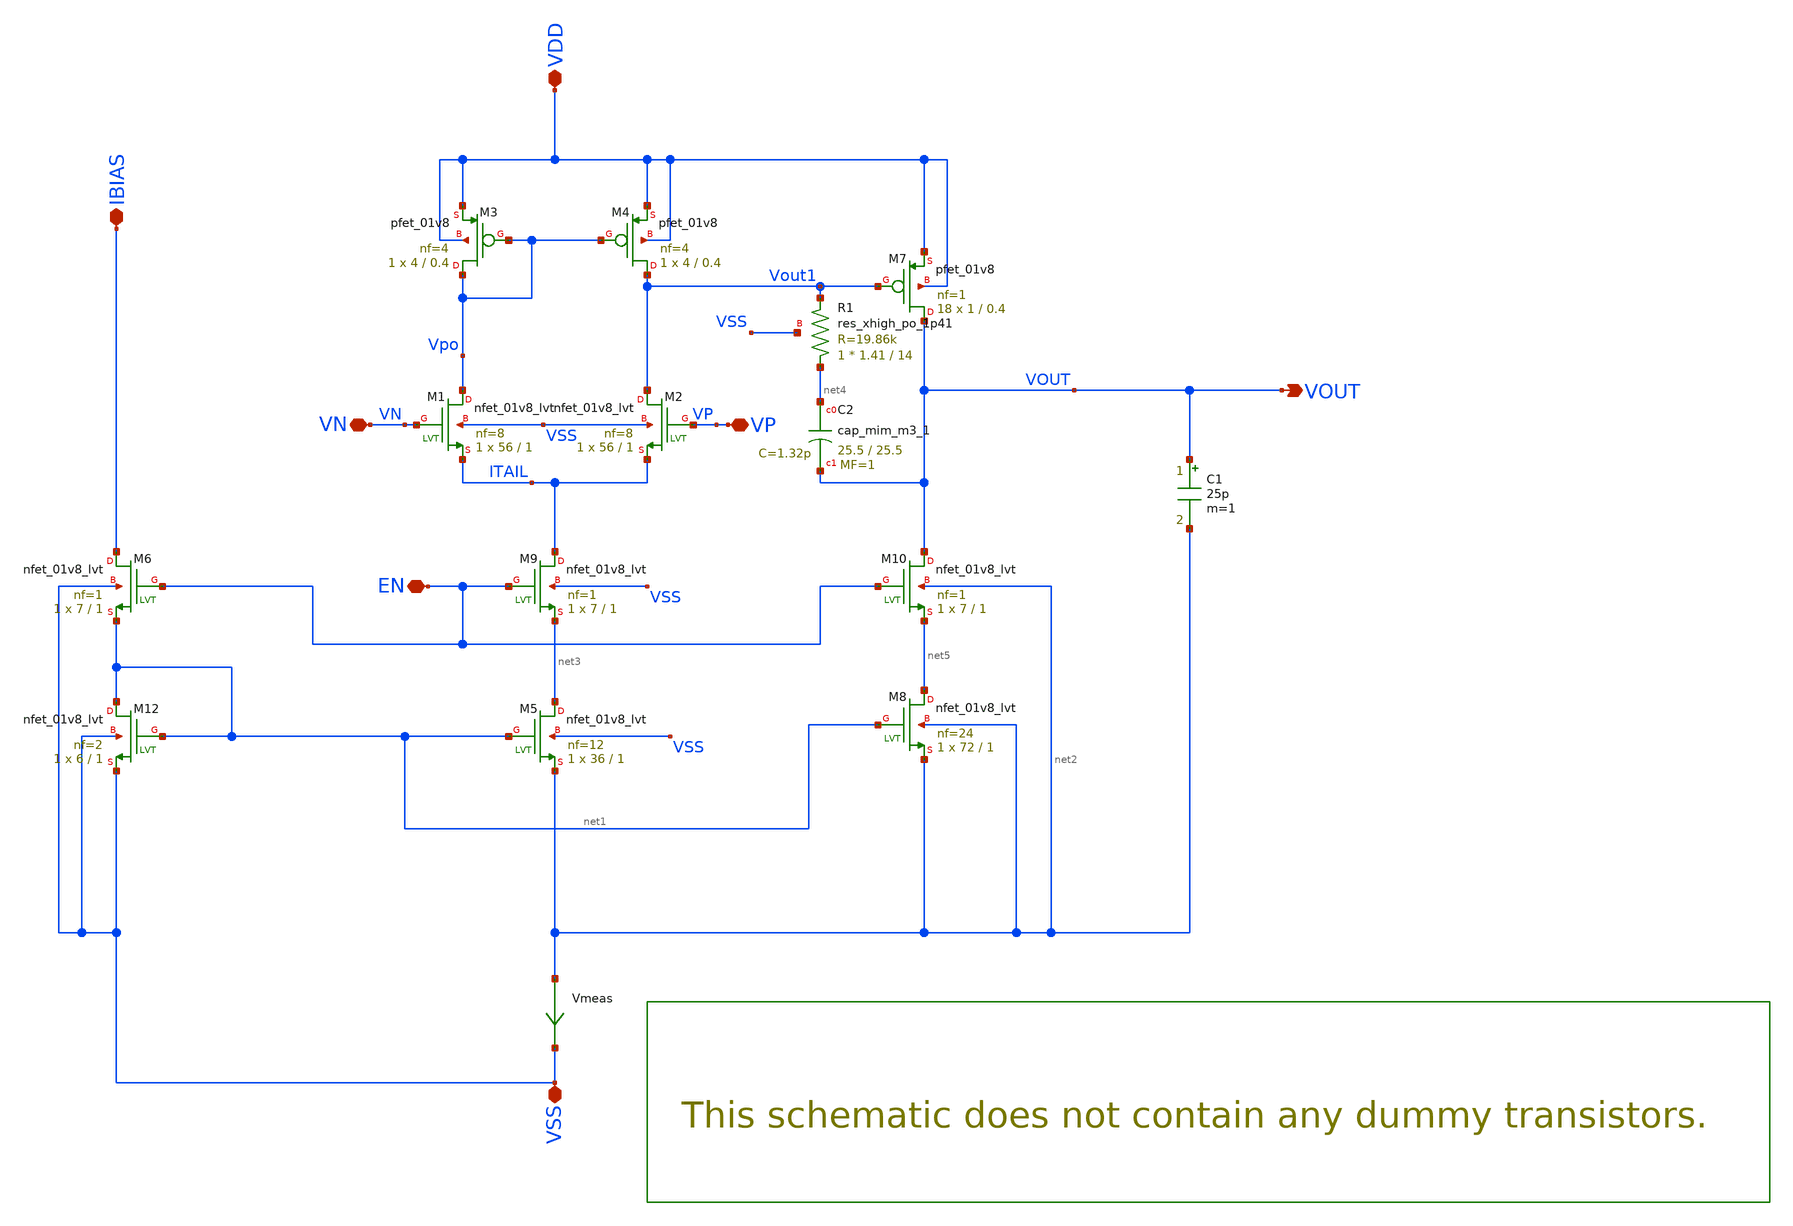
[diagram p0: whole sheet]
** sch_path: xschem/ttsky25_two_stage_opamp_tb.sch
**.subckt ttsky25_two_stage_opamp_tb VSS VDD IBIAS VOUT EN VN VP
*.iopin VSS
*.iopin VDD
*.iopin IBIAS
*.opin VOUT
*.iopin EN
*.iopin VN
*.iopin VP
C1 VOUT net2 25p m=1
XM7 VOUT Vout1 VDD VDD sky130_fd_pr__pfet_01v8 L=0.4 W=1 nf=1 ad='int((nf+1)/2) * W/nf * 0.29' as='int((nf+2)/2) * W/nf * 0.29'
+ pd='2*int((nf+1)/2) * (W/nf + 0.29)' ps='2*int((nf+2)/2) * (W/nf + 0.29)' nrd='0.29 / W' nrs='0.29 / W'
+ sa=0 sb=0 sd=0 mult=18 m=18
XM4 Vout1 Vpo VDD VDD sky130_fd_pr__pfet_01v8 L=0.4 W=4 nf=4 ad='int((nf+1)/2) * W/nf * 0.29' as='int((nf+2)/2) * W/nf * 0.29'
+ pd='2*int((nf+1)/2) * (W/nf + 0.29)' ps='2*int((nf+2)/2) * (W/nf + 0.29)' nrd='0.29 / W' nrs='0.29 / W'
+ sa=0 sb=0 sd=0 mult=1 m=1
XM3 Vpo Vpo VDD VDD sky130_fd_pr__pfet_01v8 L=0.4 W=4 nf=4 ad='int((nf+1)/2) * W/nf * 0.29' as='int((nf+2)/2) * W/nf * 0.29'
+ pd='2*int((nf+1)/2) * (W/nf + 0.29)' ps='2*int((nf+2)/2) * (W/nf + 0.29)' nrd='0.29 / W' nrs='0.29 / W'
+ sa=0 sb=0 sd=0 mult=1 m=1
Vmeas net2 VSS 0
.save i(vmeas)
XM1 Vpo VN ITAIL VSS sky130_fd_pr__nfet_01v8_lvt L=1 W=56 nf=8 ad='int((8 + 1)/2) * 56 / 8 * 0.29' as='int((8 + 2)/2) * 56 / 8 * 0.29'
+ pd='2*int((8 + 1)/2) * (56 / 8 + 0.29)' ps='2*int((8 + 2)/2) * (56 / 8 + 0.29)' nrd='0.29 / 56 ' nrs='0.29 / 56 '
+ sa=0 sb=0 sd=0 mult=1 m=1
XM2 Vout1 VP ITAIL VSS sky130_fd_pr__nfet_01v8_lvt L=1 W=56 nf=8 ad='int((8 + 1)/2) * 56 / 8 * 0.29'
+ as='int((8 + 2)/2) * 56 / 8 * 0.29' pd='2*int((8 + 1)/2) * (56 / 8 + 0.29)' ps='2*int((8 + 2)/2) * (56 / 8 + 0.29)'
+ nrd='0.29 / 56 ' nrs='0.29 / 56 ' sa=0 sb=0 sd=0 mult=1 m=1
XM12 net1 net1 VSS VSS sky130_fd_pr__nfet_01v8_lvt L=1 W=6 nf=2 ad='int((2 + 1)/2) * 6 / 2 * 0.29' as='int((2 + 2)/2) * 6 / 2 * 0.29'
+ pd='2*int((2 + 1)/2) * (6 / 2 + 0.29)' ps='2*int((2 + 2)/2) * (6 / 2 + 0.29)' nrd='0.29 / 6 ' nrs='0.29 / 6 '
+ sa=0 sb=0 sd=0 mult=1 m=1
XM5 net3 net1 net2 VSS sky130_fd_pr__nfet_01v8_lvt L=1 W=36 nf=12 ad='int((12 + 1)/2) * 36 / 12 * 0.29'
+ as='int((12 + 2)/2) * 36 / 12 * 0.29' pd='2*int((12 + 1)/2) * (36 / 12 + 0.29)' ps='2*int((12 + 2)/2) * (36 / 12 + 0.29)'
+ nrd='0.29 / 36 ' nrs='0.29 / 36 ' sa=0 sb=0 sd=0 mult=1 m=1
XM8 net5 net1 net2 net2 sky130_fd_pr__nfet_01v8_lvt L=1 W=72 nf=24 ad='int((24 + 1)/2) * 72 / 24 * 0.29'
+ as='int((24 + 2)/2) * 72 / 24 * 0.29' pd='2*int((24 + 1)/2) * (72 / 24 + 0.29)' ps='2*int((24 + 2)/2) * (72 / 24 + 0.29)'
+ nrd='0.29 / 72 ' nrs='0.29 / 72 ' sa=0 sb=0 sd=0 mult=1 m=1
XM6 IBIAS EN net1 VSS sky130_fd_pr__nfet_01v8_lvt L=1 W=7 nf=1 ad='int((1 + 1)/2) * 7 / 1 * 0.29' as='int((1 + 2)/2) * 7 / 1 * 0.29'
+ pd='2*int((1 + 1)/2) * (7 / 1 + 0.29)' ps='2*int((1 + 2)/2) * (7 / 1 + 0.29)' nrd='0.29 / 7 ' nrs='0.29 / 7 '
+ sa=0 sb=0 sd=0 mult=1 m=1
XM9 ITAIL EN net3 VSS sky130_fd_pr__nfet_01v8_lvt L=1 W=7 nf=1 ad='int((1 + 1)/2) * 7 / 1 * 0.29' as='int((1 + 2)/2) * 7 / 1 * 0.29'
+ pd='2*int((1 + 1)/2) * (7 / 1 + 0.29)' ps='2*int((1 + 2)/2) * (7 / 1 + 0.29)' nrd='0.29 / 7 ' nrs='0.29 / 7 '
+ sa=0 sb=0 sd=0 mult=1 m=1
XM10 VOUT EN net5 net2 sky130_fd_pr__nfet_01v8_lvt L=1 W=7 nf=1 ad='int((1 + 1)/2) * 7 / 1 * 0.29' as='int((1 + 2)/2) * 7 / 1 * 0.29'
+ pd='2*int((1 + 1)/2) * (7 / 1 + 0.29)' ps='2*int((1 + 2)/2) * (7 / 1 + 0.29)' nrd='0.29 / 7 ' nrs='0.29 / 7 '
+ sa=0 sb=0 sd=0 mult=1 m=1
XC2 net4 VOUT sky130_fd_pr__cap_mim_m3_1 W=25.5 L=25.5 MF=1 m=1
XR1 net4 Vout1 VSS sky130_fd_pr__res_xhigh_po_1p41 L=14 mult=1 m=1
**** begin user architecture code


.lib /foss/pdks/sky130A/libs.tech/ngspice/sky130.lib.spice tt
.param vcm = 0.9
**Setup
Vdd vdd 0 1.8
Ven en 0 1.8
Ibias Vdd Ibias 5u
*Vdd vdd 0 SIN(1.8 0.1 600k)
Vss vss 0 0

*Uncomment sources below depending*
*on what simulation needs to be run*
*AC simulation or (DC + Transient)*

*This line is not really needed -> Vdiff vdiff 0 0

*Transient + DC Transfer*
*Vdiff vdiff 0 SIN(0 0.001 1k)
*Bvp vp 0 V = vcm + V(vdiff)/2
*Bvn vn 0 V = vcm - V(vdiff)/2

*AC small signal*
Vp vp 0 vcm AC 0.001
Vn vn 0 vcm AC -0.001

**Simulation
.option temp=27 gmin=1e-12
.save all
.options savecurrents
.control
** Define input signal
let fsig = 1k
let tper = 1/fsig
** Define transient params
let tstop = 10*tper
let tstep = 0.001*tper

op
remzerovec
write ttsky25_two_stage_opamp_tb.raw
echo ---xm2---
let gds2 = @m.xm2.msky130_fd_pr__nfet_01v8_lvt[gds]
let ro2 = 1/gds2
echo ---xm4---
let gds4 = @m.xm4.msky130_fd_pr__pfet_01v8[gds]
let ro4 = 1/gds4
let RoD = 1/((1/ro2) + (1/ro4))
echo ---xm6---
print @m.xm6.msky130_fd_pr__nfet_01v8_lvt[vdsat]
echo -----COMMON SOURCE-----
echo ---xm7---
let gds7 = @m.xm7.msky130_fd_pr__pfet_01v8[gds]
let gm7 = @m.xm7.msky130_fd_pr__pfet_01v8[gm]
let r_zero = 1/gm7
print r_zero
let ro7 = 1/gds7
echo ---xm8---
let gds8 = @m.xm8.msky130_fd_pr__nfet_01v8_lvt[gds]
let ro8 = 1/gds8
echo ---xm10---
let gds10 = @m.xm10.msky130_fd_pr__nfet_01v8_lvt[gds]
let ro10 = 1/gds10
let Ros = 1/((1/ro7) + (1/(ro8+ro10)))


tran $&tstep $&tstop
let current = -i(vdd)
plot vp vn vout1
plot vp vn vout

dc vdiff -0.9 0.9 10m
let vin = vp -vn
plot vin vout1 vdd
meas dc vout1_at_zero find vout1 when vdiff=0

dc vdiff -0.9 0.9 10m
let vin = vp -vn
plot vin vout vdd
meas dc vout_at_zero find vout when vdiff=0

ac dec 200 10 10000Meg
let vin = vp - vn
let gain = db(vout/vin)
let phase_deg = 180*cph(vout/vin)/pi
plot gain phase_deg xlog
meas ac gain_max MAX gain
let db_3 = gain_max - 3
print db_3
meas ac f_pole WHEN gain = db_3
meas ac f_u WHEN gain = 0
meas ac gain_10k FIND gain AT=10e3
meas ac phase_at_fu FIND phase_deg AT=f_u
let phase_margin = 180 + phase_at_fu
print phase_margin
setplot op1
print @m.xm2.msky130_fd_pr__nfet_01v8_lvt[vth]
print @m.xm2.msky130_fd_pr__nfet_01v8_lvt[gm]
print @m.xm2.msky130_fd_pr__nfet_01v8_lvt[vdsat]
print @m.xm7.msky130_fd_pr__pfet_01v8[vth]
print @m.xm7.msky130_fd_pr__pfet_01v8[gm]
print @m.xm7.msky130_fd_pr__pfet_01v8[vdsat]
print @m.xm4.msky130_fd_pr__pfet_01v8[vth]
print @m.xm4.msky130_fd_pr__pfet_01v8[gm]
print @m.xm4.msky130_fd_pr__pfet_01v8[vdsat]
print ro2
print ro4
print RoD
print ro10
print ro8
print ro8+ro10
print ro7
print Ros
let ro5 = 1/@m.xm5.msky130_fd_pr__nfet_01v8_lvt[gds]
print ro5
let Av1 = @m.xm2.msky130_fd_pr__nfet_01v8_lvt[gm] * RoD
let Av2 = @m.xm7.msky130_fd_pr__pfet_01v8[gm] * Ros
print Av1
print Av2
let x7_gm_id = @m.xm7.msky130_fd_pr__pfet_01v8[gm]/@m.xm7.msky130_fd_pr__pfet_01v8[id]
print x7_gm_id
let x4_gm_id = @m.xm4.msky130_fd_pr__pfet_01v8[gm]/@m.xm4.msky130_fd_pr__pfet_01v8[id]
print x4_gm_id
let x2_gm_id = @m.xm2.msky130_fd_pr__nfet_01v8_lvt[gm]/@m.xm2.msky130_fd_pr__nfet_01v8_lvt[id]
print x2_gm_id
.endc


**** end user architecture code
**.ends
.end
